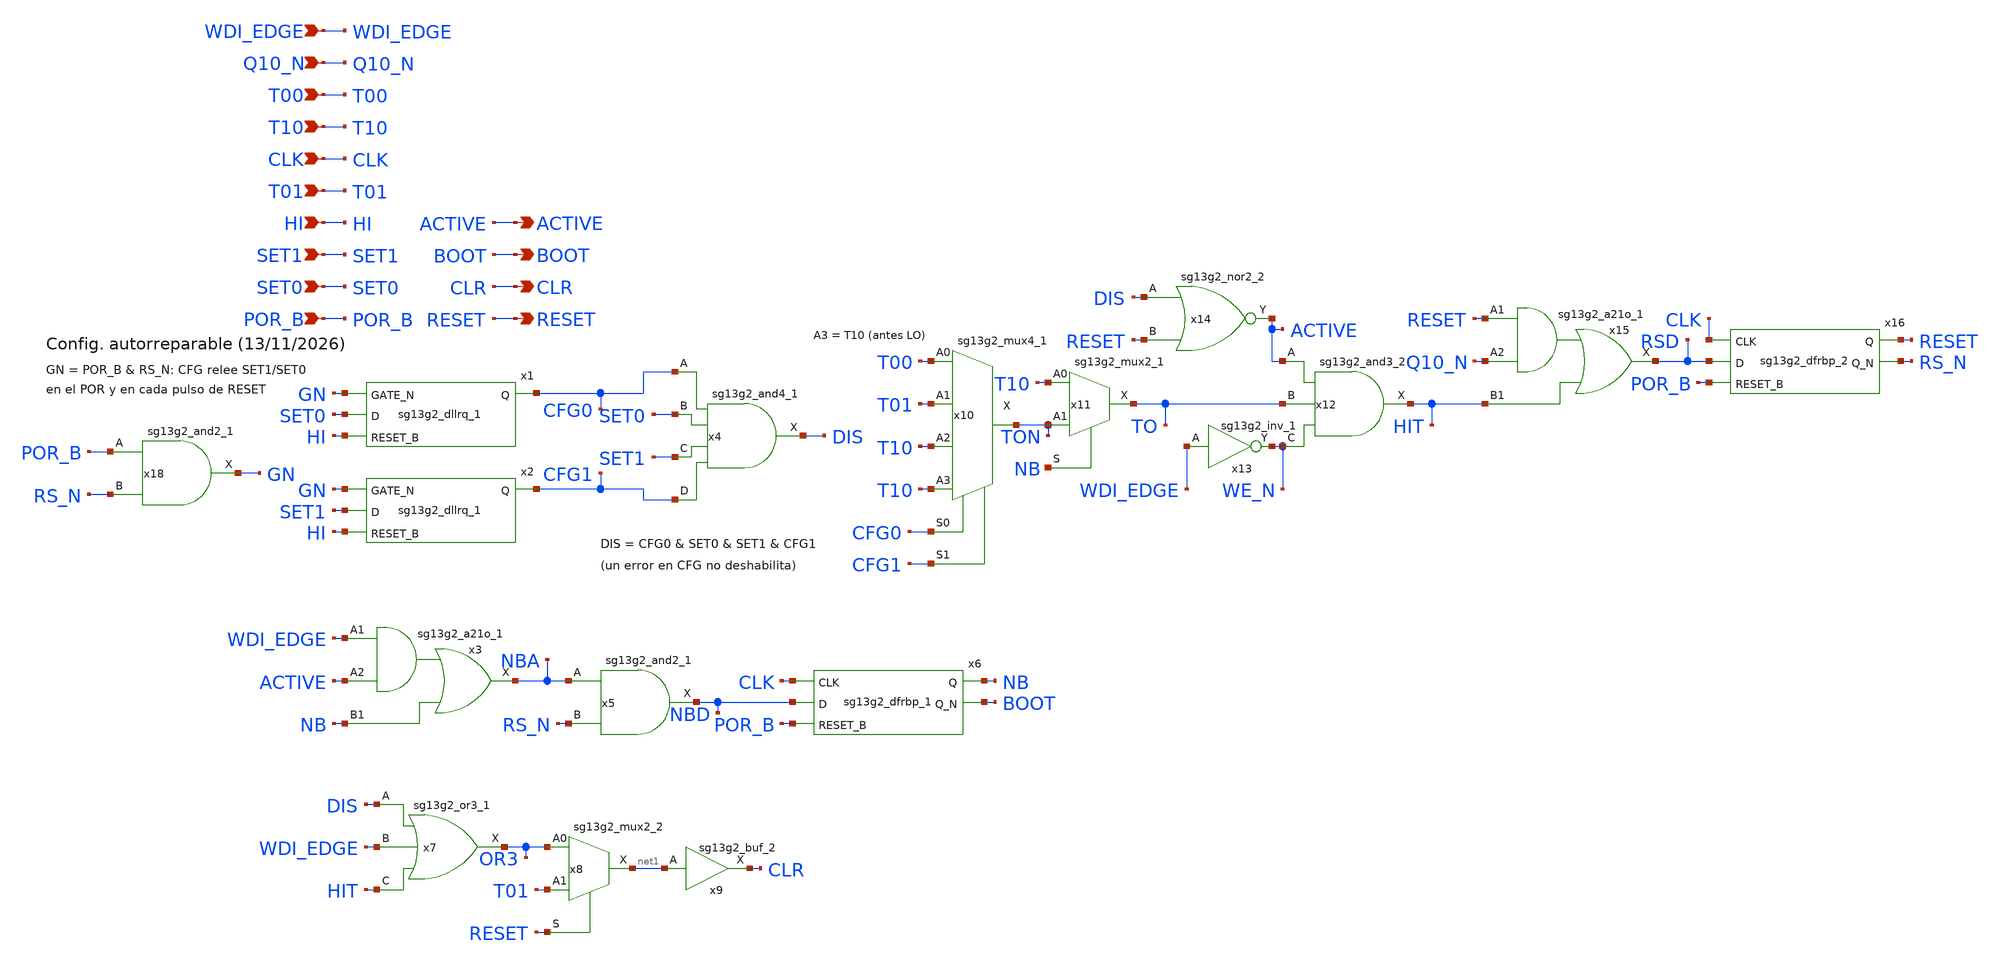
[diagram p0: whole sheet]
** sch_path: design/blocks/digital/schematic/wd_control.sch
* IHP-GmbH/IHP-Open-PDK/ihp-sg13g2/libs.tech/xschem/sg13g2_stdcells/sg13g2_a21o_1.sch:
* Copyright 2023 IHP PDK Authors
* Licensed under the Apache License, Version 2.0 (the "License");
**.subckt wd_control POR_B SET0 CLR RESET SET1 HI T01 ACTIVE BOOT CLK T10 T00 Q10_N WDI_EDGE
*.ipin POR_B
*.ipin SET0
*.opin CLR
*.opin RESET
*.ipin SET1
*.ipin HI
*.ipin T01
*.opin ACTIVE
*.opin BOOT
*.ipin CLK
*.ipin T10
*.ipin T00
*.ipin Q10_N
*.ipin WDI_EDGE
x1 SET0 HI VGND VNB VPB VPWR CFG0 sg13g2_dllrq_1
x2 SET1 HI VGND VNB VPB VPWR CFG1 sg13g2_dllrq_1
x3 NBA WDI_EDGE ACTIVE NB VDD VSS sg13g2_a21o_1
x5 NBD NBA RS_N VDD VSS sg13g2_and2_1
x6 NB BOOT CLK NBD POR_B VDD VSS sg13g2_dfrbp_1
x7 OR3 DIS WDI_EDGE HIT VDD VSS sg13g2_or3_1
x8 net1 OR3 T01 RESET VDD VSS sg13g2_mux2_2
x9 CLR net1 VDD VSS sg13g2_buf_2
x10 TON T00 T01 T10 T10 CFG0 CFG1 VDD VSS sg13g2_mux4_1
x11 TO T10 TON NB VDD VSS sg13g2_mux2_1
x12 HIT ACTIVE TO WE_N VDD VSS sg13g2_and3_2
x13 WE_N WDI_EDGE VDD VSS sg13g2_inv_1
x14 ACTIVE DIS RESET VDD VSS sg13g2_nor2_2
x15 RSD RESET Q10_N HIT VDD VSS sg13g2_a21o_1
x16 RESET RS_N CLK RSD POR_B VDD VSS sg13g2_dfrbp_2
x4 DIS CFG0 SET0 SET1 CFG1 VDD VSS sg13g2_and4_1
x18 GN POR_B RS_N VDD VSS sg13g2_and2_1
**.ends

* expanding   symbol:  sg13g2_a21o_1.sym # of pins=4
** sym_path: sg13g2_a21o_1.sym
** sch_path: sg13g2_a21o_1.sch
.subckt sg13g2_a21o_1 X A1 A2 B1 VDD VSS
*.opin X
*.ipin A1
*.ipin A2
*.ipin B1
*.iopin VDD
*.iopin VSS
XM1 net1 A1 net3 VSS sg13_lv_nmos w=640.00n l=130.00n ng=1 m=1 mm_ok=1
XM2 net3 A2 VSS VSS sg13_lv_nmos w=640.00n l=130.00n ng=1 m=1 mm_ok=1
XM3 net1 B1 VSS VSS sg13_lv_nmos w=640.00n l=130.00n ng=1 m=1 mm_ok=1
XM4 X net1 VSS VSS sg13_lv_nmos w=740.00n l=130.00n ng=1 m=1 mm_ok=1
XM5 net2 A1 VDD VDD sg13_lv_pmos w=1.000u l=130.00n ng=1 m=1 mm_ok=1
XM6 net2 A2 VDD VDD sg13_lv_pmos w=1.000u l=130.00n ng=1 m=1 mm_ok=1
XM7 net1 B1 net2 VDD sg13_lv_pmos w=1.000u l=130.00n ng=1 m=1 mm_ok=1
XM8 X net1 VDD VDD sg13_lv_pmos w=1.12u l=130.00n ng=1 m=1 mm_ok=1
.ends


* expanding   symbol:  sg13g2_and2_1.sym # of pins=3
** sym_path: sg13g2_and2_1.sym
** sch_path: sg13g2_and2_1.sch
.subckt sg13g2_and2_1 X A B VDD VSS
*.ipin A
*.ipin B
*.opin X
*.iopin VDD
*.iopin VSS
XM1 net1 A net2 VSS sg13_lv_nmos w=640.00n l=130.00n ng=1 m=1 mm_ok=1
XM2 net2 B VSS VSS sg13_lv_nmos w=640.00n l=130.00n ng=1 m=1 mm_ok=1
XM3 X net1 VSS VSS sg13_lv_nmos w=740.00n l=130.00n ng=1 m=1 mm_ok=1
XM4 net1 B VDD VDD sg13_lv_pmos w=840.00n l=130.00n ng=1 m=1 mm_ok=1
XM5 net1 A VDD VDD sg13_lv_pmos w=840.00n l=130.00n ng=1 m=1 mm_ok=1
XM6 X net1 VDD VDD sg13_lv_pmos w=1.12u l=130.00n ng=1 m=1 mm_ok=1
.ends


* expanding   symbol:  sg13g2_dfrbp_1.sym # of pins=5
** sym_path: sg13g2_dfrbp_1.sym
** sch_path: sg13g2_dfrbp_1.sch
.subckt sg13g2_dfrbp_1 Q Q_N CLK D RESET_B VDD VSS
*.ipin D
*.ipin RESET_B
*.ipin CLK
*.opin Q
*.opin Q_N
*.iopin VDD
*.iopin VSS
XM1 Db D net10 VSS sg13_lv_nmos w=420.00n l=130.00n ng=1 m=1 mm_ok=1
XM2 net10 RESET_B VSS VSS sg13_lv_nmos w=420.00n l=130.00n ng=1 m=1 mm_ok=1
XM3 net1 clkneg net9 VSS sg13_lv_nmos w=420.00n l=130.00n ng=1 m=1 mm_ok=1
XM4 net9 net1 VSS VSS sg13_lv_nmos w=420.00n l=130.00n ng=1 m=1 mm_ok=1
XM5 net1 net1 net5 VSS sg13_lv_nmos w=420.00n l=130.00n ng=1 m=1 mm_ok=1
XM6 net5 RESET_B VSS VSS sg13_lv_nmos w=420.00n l=130.00n ng=1 m=1 mm_ok=1
XM7 Q_N net1 VSS VSS sg13_lv_nmos w=740.00n l=130.00n ng=1 m=1 mm_ok=1
XM8 net2 net1 VSS VSS sg13_lv_nmos w=740.00n l=130.00n ng=1 m=1 mm_ok=1
XM9 Q net2 VSS VSS sg13_lv_nmos w=740.00n l=130.00n ng=1 m=1 mm_ok=1
XM10 clkneg CLK VSS VSS sg13_lv_nmos w=740.00n l=130.00n ng=1 m=1 mm_ok=1
XM11 clkpos clkneg VSS VSS sg13_lv_nmos w=740.00n l=130.00n ng=1 m=1 mm_ok=1
XM12 Db clkneg net3 VSS sg13_lv_nmos w=420.00n l=130.00n ng=1 m=1 mm_ok=1
XM13 net3 clkpos net8 VSS sg13_lv_nmos w=420.00n l=130.00n ng=1 m=1 mm_ok=1
XM14 net8 net3 net4 VSS sg13_lv_nmos w=420.00n l=130.00n ng=1 m=1 mm_ok=1
XM15 net4 RESET_B VSS VSS sg13_lv_nmos w=420.00n l=130.00n ng=1 m=1 mm_ok=1
XM16 net3 net3 VSS VSS sg13_lv_nmos w=740.00n l=130.00n ng=1 m=1 mm_ok=1
XM17 net3 clkpos net1 VSS sg13_lv_nmos w=740.00n l=130.00n ng=1 m=1 mm_ok=1
XM18 Db RESET_B VDD VDD sg13_lv_pmos w=420.00n l=130.00n ng=1 m=1 mm_ok=1
XM19 Db D VDD VDD sg13_lv_pmos w=420.00n l=130.00n ng=1 m=1 mm_ok=1
XM20 net7 net1 VDD VDD sg13_lv_pmos w=420.00n l=130.00n ng=1 m=1 mm_ok=1
XM21 net1 clkpos net7 VDD sg13_lv_pmos w=420.00n l=130.00n ng=1 m=1 mm_ok=1
XM22 net1 net1 VDD VDD sg13_lv_pmos w=420.00n l=130.00n ng=1 m=1 mm_ok=1
XM23 net1 RESET_B VDD VDD sg13_lv_pmos w=420.00n l=130.00n ng=1 m=1 mm_ok=1
XM24 Q_N net1 VDD VDD sg13_lv_pmos w=1.12u l=130.00n ng=1 m=1 mm_ok=1
XM25 net2 net1 VDD VDD sg13_lv_pmos w=1.12u l=130.00n ng=1 m=1 mm_ok=1
XM26 Q net2 VDD VDD sg13_lv_pmos w=1.12u l=130.00n ng=1 m=1 mm_ok=1
XM27 clkneg CLK VDD VDD sg13_lv_pmos w=1.12u l=130.00n ng=1 m=1 mm_ok=1
XM28 clkpos clkneg VDD VDD sg13_lv_pmos w=1.12u l=130.00n ng=1 m=1 mm_ok=1
XM29 Db clkpos net3 VDD sg13_lv_pmos w=420.00n l=130.00n ng=1 m=1 mm_ok=1
XM30 net6 net3 VDD VDD sg13_lv_pmos w=420.00n l=130.00n ng=1 m=1 mm_ok=1
XM31 net3 clkneg net6 VDD sg13_lv_pmos w=420.00n l=130.00n ng=1 m=1 mm_ok=1
XM32 net3 RESET_B VDD VDD sg13_lv_pmos w=420.00n l=130.00n ng=1 m=1 mm_ok=1
XM33 net3 net3 VDD VDD sg13_lv_pmos w=1.000u l=130.00n ng=1 m=1 mm_ok=1
XM34 net3 clkneg net1 VDD sg13_lv_pmos w=1.000u l=130.00n ng=1 m=1 mm_ok=1
.ends


* expanding   symbol:  sg13g2_or3_1.sym # of pins=4
** sym_path: sg13g2_or3_1.sym
** sch_path: sg13g2_or3_1.sch
.subckt sg13g2_or3_1 X A B C VDD VSS
*.opin X
*.ipin C
*.ipin B
*.ipin A
*.iopin VDD
*.iopin VSS
XM1 net2 A VSS VSS sg13_lv_nmos w=550.00n l=130.00n ng=1 m=1 mm_ok=1
XM2 net2 B VSS VSS sg13_lv_nmos w=550.00n l=130.00n ng=1 m=1 mm_ok=1
XM3 net2 C VSS VSS sg13_lv_nmos w=550.00n l=130.00n ng=1 m=1 mm_ok=1
XM4 X net2 VSS VSS sg13_lv_nmos w=740.00n l=130.00n ng=1 m=1 mm_ok=1
XM5 net1 A VDD VDD sg13_lv_pmos w=1.000u l=130.00n ng=1 m=1 mm_ok=1
XM6 net3 B net1 VDD sg13_lv_pmos w=1.000u l=130.00n ng=1 m=1 mm_ok=1
XM7 net2 C net3 VDD sg13_lv_pmos w=1.000u l=130.00n ng=1 m=1 mm_ok=1
XM8 X net2 VDD VDD sg13_lv_pmos w=1.12u l=130.00n ng=1 m=1 mm_ok=1
.ends


* expanding   symbol:  sg13g2_mux2_2.sym # of pins=4
** sym_path: sg13g2_mux2_2.sym
** sch_path: sg13g2_mux2_2.sch
.subckt sg13g2_mux2_2 X A0 A1 S VDD VSS
*.ipin S
*.ipin A0
*.ipin A1
*.opin X
*.iopin VDD
*.iopin VSS
XM1 Sb S VSS VSS sg13_lv_nmos w=550.00n l=130.00n ng=1 m=1 mm_ok=1
XM2 net1 A0 net5 VSS sg13_lv_nmos w=740.00n l=130.00n ng=1 m=1 mm_ok=1
XM3 net5 Sb VSS VSS sg13_lv_nmos w=740.00n l=130.00n ng=1 m=1 mm_ok=1
XM4 net1 A1 net4 VSS sg13_lv_nmos w=740.00n l=130.00n ng=1 m=1 mm_ok=1
XM5 net4 S VSS VSS sg13_lv_nmos w=740.00n l=130.00n ng=1 m=1 mm_ok=1
XM6 X net1 VSS VSS sg13_lv_nmos w=1.48u l=130.00n ng=2 m=1 mm_ok=1
XM7 Sb S VDD VDD sg13_lv_pmos w=840.00n l=130.00n ng=1 m=1 mm_ok=1
XM8 net2 S VDD VDD sg13_lv_pmos w=1.000u l=130.00n ng=1 m=1 mm_ok=1
XM9 net1 A0 net2 VDD sg13_lv_pmos w=1.000u l=130.00n ng=1 m=1 mm_ok=1
XM10 net3 Sb VDD VDD sg13_lv_pmos w=1.000u l=130.00n ng=1 m=1 mm_ok=1
XM11 net1 A1 net3 VDD sg13_lv_pmos w=1.000u l=130.00n ng=1 m=1 mm_ok=1
XM12 X net1 VDD VDD sg13_lv_pmos w=2.24u l=130.00n ng=2 m=1 mm_ok=1
.ends


* expanding   symbol:  sg13g2_buf_2.sym # of pins=2
** sym_path: sg13g2_buf_2.sym
** sch_path: sg13g2_buf_2.sch
.subckt sg13g2_buf_2 X A VDD VSS
*.ipin A
*.opin X
*.iopin VDD
*.iopin VSS
XM1 net1 A VSS VSS sg13_lv_nmos w=640.00n l=130.00n ng=1 m=1 mm_ok=1
XM2 X net1 VSS VSS sg13_lv_nmos w=1.48u l=130.00n ng=2 m=1 mm_ok=1
XM3 net1 A VDD VDD sg13_lv_pmos w=1.000u l=130.00n ng=1 m=1 mm_ok=1
XM4 X net1 VDD VDD sg13_lv_pmos w=2.24u l=130.00n ng=2 m=1 mm_ok=1
.ends


* expanding   symbol:  sg13g2_mux4_1.sym # of pins=7
** sym_path: sg13g2_mux4_1.sym
** sch_path: sg13g2_mux4_1.sch
.subckt sg13g2_mux4_1 X A0 A1 A2 A3 S0 S1 VDD VSS
*.ipin S0
*.ipin S1
*.iopin VSS
*.ipin A0
*.ipin A1
*.ipin A2
*.ipin A3
*.opin X
*.iopin VDD
XM1 S0b S0 VSS VSS sg13_lv_nmos w=640.00n l=130.00n ng=1 m=1 mm_ok=1
XM2 S1b S1 VSS VSS sg13_lv_nmos w=640.00n l=130.00n ng=1 m=1 mm_ok=1
XM3 net4 A3 VSS VSS sg13_lv_nmos w=640.00n l=130.00n ng=1 m=1 mm_ok=1
XM4 high S1 Xb VSS sg13_lv_nmos w=640.00n l=130.00n ng=1 m=1 mm_ok=1
XM5 X Xb VSS VSS sg13_lv_nmos w=740.00n l=130.00n ng=1 m=1 mm_ok=1
XM6 low S0b net7 VSS sg13_lv_nmos w=640.00n l=130.00n ng=1 m=1 mm_ok=1
XM7 net7 A0 VSS VSS sg13_lv_nmos w=640.00n l=130.00n ng=1 m=1 mm_ok=1
XM8 low S0 net2 VSS sg13_lv_nmos w=640.00n l=130.00n ng=1 m=1 mm_ok=1
XM9 net2 A1 VSS VSS sg13_lv_nmos w=640.00n l=130.00n ng=1 m=1 mm_ok=1
XM10 low S1b Xb VSS sg13_lv_nmos w=640.00n l=130.00n ng=1 m=1 mm_ok=1
XM11 high S0b net6 VSS sg13_lv_nmos w=640.00n l=130.00n ng=1 m=1 mm_ok=1
XM12 net6 A2 VSS VSS sg13_lv_nmos w=640.00n l=130.00n ng=1 m=1 mm_ok=1
XM13 high S0 net4 VSS sg13_lv_nmos w=640.00n l=130.00n ng=1 m=1 mm_ok=1
XM14 S0b S0 VDD VDD sg13_lv_pmos w=1.000u l=130.00n ng=1 m=1 mm_ok=1
XM15 S1b S1 VDD VDD sg13_lv_pmos w=1.000u l=130.00n ng=1 m=1 mm_ok=1
XM16 high S0b net3 VDD sg13_lv_pmos w=1.000u l=130.00n ng=1 m=1 mm_ok=1
XM17 high S1b Xb VDD sg13_lv_pmos w=1.000u l=130.00n ng=1 m=1 mm_ok=1
XM18 X Xb VDD VDD sg13_lv_pmos w=1.12u l=130.00n ng=1 m=1 mm_ok=1
XM19 net8 A0 VDD VDD sg13_lv_pmos w=1.000u l=130.00n ng=1 m=1 mm_ok=1
XM20 low S0 net8 VDD sg13_lv_pmos w=1.000u l=130.00n ng=1 m=1 mm_ok=1
XM21 net1 A1 VDD VDD sg13_lv_pmos w=1.000u l=130.00n ng=1 m=1 mm_ok=1
XM22 low S0b net1 VDD sg13_lv_pmos w=1.000u l=130.00n ng=1 m=1 mm_ok=1
XM23 low S1 Xb VDD sg13_lv_pmos w=1.000u l=130.00n ng=1 m=1 mm_ok=1
XM24 net5 A2 VDD VDD sg13_lv_pmos w=1.000u l=130.00n ng=1 m=1 mm_ok=1
XM25 high S0 net5 VDD sg13_lv_pmos w=1.000u l=130.00n ng=1 m=1 mm_ok=1
XM26 net3 A3 VDD VDD sg13_lv_pmos w=1.000u l=130.00n ng=1 m=1 mm_ok=1
.ends


* expanding   symbol:  sg13g2_mux2_1.sym # of pins=4
** sym_path: sg13g2_mux2_1.sym
** sch_path: sg13g2_mux2_1.sch
.subckt sg13g2_mux2_1 X A0 A1 S VDD VSS
*.ipin S
*.ipin A0
*.ipin A1
*.opin X
*.iopin VDD
*.iopin VSS
XM1 Sb S VSS VSS sg13_lv_nmos w=550.00n l=130.00n ng=1 m=1 mm_ok=1
XM2 net1 A0 net5 VSS sg13_lv_nmos w=740.00n l=130.00n ng=1 m=1 mm_ok=1
XM3 net5 Sb VSS VSS sg13_lv_nmos w=740.00n l=130.00n ng=1 m=1 mm_ok=1
XM4 net1 A1 net4 VSS sg13_lv_nmos w=740.00n l=130.00n ng=1 m=1 mm_ok=1
XM5 net4 S VSS VSS sg13_lv_nmos w=740.00n l=130.00n ng=1 m=1 mm_ok=1
XM6 X net1 VSS VSS sg13_lv_nmos w=740.00n l=130.00n ng=1 m=1 mm_ok=1
XM7 Sb S VDD VDD sg13_lv_pmos w=840.00n l=130.00n ng=1 m=1 mm_ok=1
XM8 net2 S VDD VDD sg13_lv_pmos w=1.000u l=130.00n ng=1 m=1 mm_ok=1
XM9 net1 A0 net2 VDD sg13_lv_pmos w=1.000u l=130.00n ng=1 m=1 mm_ok=1
XM10 net3 Sb VDD VDD sg13_lv_pmos w=1.000u l=130.00n ng=1 m=1 mm_ok=1
XM11 net1 A1 net3 VDD sg13_lv_pmos w=1.000u l=130.00n ng=1 m=1 mm_ok=1
XM12 X net1 VDD VDD sg13_lv_pmos w=1.12u l=130.00n ng=1 m=1 mm_ok=1
.ends


* expanding   symbol:  sg13g2_and3_2.sym # of pins=4
** sym_path: sg13g2_and3_2.sym
** sch_path: sg13g2_and3_2.sch
.subckt sg13g2_and3_2 X A B C VDD VSS
*.opin X
*.ipin C
*.ipin B
*.ipin A
*.iopin VDD
*.iopin VSS
XM1 net1 A net3 VSS sg13_lv_nmos w=640.00n l=130.00n ng=1 m=1 mm_ok=1
XM2 net3 B net2 VSS sg13_lv_nmos w=640.00n l=130.00n ng=1 m=1 mm_ok=1
XM3 net2 C VSS VSS sg13_lv_nmos w=640.00n l=130.00n ng=1 m=1 mm_ok=1
XM4 X net1 VSS VSS sg13_lv_nmos w=1.48u l=130.00n ng=2 m=1 mm_ok=1
XM5 net1 C VDD VDD sg13_lv_pmos w=840.00n l=130.00n ng=1 m=1 mm_ok=1
XM6 net1 B VDD VDD sg13_lv_pmos w=840.00n l=130.00n ng=1 m=1 mm_ok=1
XM7 net1 A VDD VDD sg13_lv_pmos w=840.00n l=130.00n ng=1 m=1 mm_ok=1
XM8 X net1 VDD VDD sg13_lv_pmos w=2.24u l=130.00n ng=2 m=1 mm_ok=1
.ends


* expanding   symbol:  sg13g2_inv_1.sym # of pins=2
** sym_path: sg13g2_inv_1.sym
** sch_path: sg13g2_inv_1.sch
.subckt sg13g2_inv_1 Y A VDD VSS
*.opin Y
*.ipin A
*.iopin VDD
*.iopin VSS
XM1 Y A VSS VSS sg13_lv_nmos w=740.00n l=130.00n ng=1 m=1 mm_ok=1
XM2 Y A VDD VDD sg13_lv_pmos w=1.12u l=130.00n ng=1 m=1 mm_ok=1
.ends


* expanding   symbol:  sg13g2_nor2_2.sym # of pins=3
** sym_path: sg13g2_nor2_2.sym
** sch_path: sg13g2_nor2_2.sch
.subckt sg13g2_nor2_2 Y A B VDD VSS
*.opin Y
*.ipin B
*.ipin A
*.iopin VDD
*.iopin VSS
XM1 Y A VSS VSS sg13_lv_nmos w=1.48u l=130.00n ng=2 m=1 mm_ok=1
XM2 Y B VSS VSS sg13_lv_nmos w=1.48u l=130.00n ng=2 m=1 mm_ok=1
XM3 net1 A VDD VDD sg13_lv_pmos w=2.24u l=130.00n ng=2 m=1 mm_ok=1
XM4 Y B net1 VDD sg13_lv_pmos w=2.24u l=130.00n ng=2 m=1 mm_ok=1
.ends


* expanding   symbol:  sg13g2_dfrbp_2.sym # of pins=5
** sym_path: sg13g2_dfrbp_2.sym
** sch_path: sg13g2_dfrbp_2.sch
.subckt sg13g2_dfrbp_2 Q Q_N CLK D RESET_B VDD VSS
*.ipin D
*.ipin RESET_B
*.ipin CLK
*.opin Q
*.opin Q_N
*.iopin VDD
*.iopin VSS
XM1 Db D net12 VSS sg13_lv_nmos w=420.00n l=130.00n ng=1 m=1 mm_ok=1
XM2 net12 RESET_B VSS VSS sg13_lv_nmos w=420.00n l=130.00n ng=1 m=1 mm_ok=1
XM3 net2 clkneg net11 VSS sg13_lv_nmos w=420.00n l=130.00n ng=1 m=1 mm_ok=1
XM4 net11 net3 VSS VSS sg13_lv_nmos w=420.00n l=130.00n ng=1 m=1 mm_ok=1
XM5 net3 net2 net7 VSS sg13_lv_nmos w=420.00n l=130.00n ng=1 m=1 mm_ok=1
XM6 net7 RESET_B VSS VSS sg13_lv_nmos w=420.00n l=130.00n ng=1 m=1 mm_ok=1
XM7 Q_N net2 VSS VSS sg13_lv_nmos w=1.48u l=130.00n ng=2 m=1 mm_ok=1
XM8 net1 net2 VSS VSS sg13_lv_nmos w=640.00n l=130.00n ng=1 m=1 mm_ok=1
XM9 Q net1 VSS VSS sg13_lv_nmos w=1.48u l=130.00n ng=2 m=1 mm_ok=1
XM10 clkneg CLK VSS VSS sg13_lv_nmos w=740.00n l=130.00n ng=1 m=1 mm_ok=1
XM11 clkpos clkneg VSS VSS sg13_lv_nmos w=740.00n l=130.00n ng=1 m=1 mm_ok=1
XM12 Db clkneg net4 VSS sg13_lv_nmos w=420.00n l=130.00n ng=1 m=1 mm_ok=1
XM13 net4 clkpos net10 VSS sg13_lv_nmos w=420.00n l=130.00n ng=1 m=1 mm_ok=1
XM14 net10 net5 net6 VSS sg13_lv_nmos w=420.00n l=130.00n ng=1 m=1 mm_ok=1
XM15 net6 RESET_B VSS VSS sg13_lv_nmos w=420.00n l=130.00n ng=1 m=1 mm_ok=1
XM16 net5 net4 VSS VSS sg13_lv_nmos w=740.00n l=130.00n ng=1 m=1 mm_ok=1
XM17 net5 clkpos net2 VSS sg13_lv_nmos w=740.00n l=130.00n ng=1 m=1 mm_ok=1
XM18 Db RESET_B VDD VDD sg13_lv_pmos w=420.00n l=130.00n ng=1 m=1 mm_ok=1
XM19 Db D VDD VDD sg13_lv_pmos w=420.00n l=130.00n ng=1 m=1 mm_ok=1
XM20 net9 net3 VDD VDD sg13_lv_pmos w=420.00n l=130.00n ng=1 m=1 mm_ok=1
XM21 net2 clkpos net9 VDD sg13_lv_pmos w=420.00n l=130.00n ng=1 m=1 mm_ok=1
XM22 net3 net2 VDD VDD sg13_lv_pmos w=420.00n l=130.00n ng=1 m=1 mm_ok=1
XM23 net3 RESET_B VDD VDD sg13_lv_pmos w=420.00n l=130.00n ng=1 m=1 mm_ok=1
XM24 Q_N net2 VDD VDD sg13_lv_pmos w=2.24u l=130.00n ng=2 m=1 mm_ok=1
XM25 net1 net2 VDD VDD sg13_lv_pmos w=1.000u l=130.00n ng=1 m=1 mm_ok=1
XM26 Q net1 VDD VDD sg13_lv_pmos w=2.24u l=130.00n ng=2 m=1 mm_ok=1
XM27 clkneg CLK VDD VDD sg13_lv_pmos w=1.12u l=130.00n ng=1 m=1 mm_ok=1
XM28 clkpos clkneg VDD VDD sg13_lv_pmos w=1.12u l=130.00n ng=1 m=1 mm_ok=1
XM29 Db clkpos net4 VDD sg13_lv_pmos w=420.00n l=130.00n ng=1 m=1 mm_ok=1
XM30 net8 net5 VDD VDD sg13_lv_pmos w=420.00n l=130.00n ng=1 m=1 mm_ok=1
XM31 net4 clkneg net8 VDD sg13_lv_pmos w=420.00n l=130.00n ng=1 m=1 mm_ok=1
XM32 net4 RESET_B VDD VDD sg13_lv_pmos w=420.00n l=130.00n ng=1 m=1 mm_ok=1
XM33 net5 net4 VDD VDD sg13_lv_pmos w=1.000u l=130.00n ng=1 m=1 mm_ok=1
XM34 net5 clkneg net2 VDD sg13_lv_pmos w=1.000u l=130.00n ng=1 m=1 mm_ok=1
.ends


* expanding   symbol:  sg13g2_and4_1.sym # of pins=5
** sym_path: sg13g2_and4_1.sym
** sch_path: sg13g2_and4_1.sch
.subckt sg13g2_and4_1 X A B C D VDD VSS
*.ipin A
*.ipin B
*.ipin C
*.ipin D
*.opin X
*.iopin VDD
*.iopin VSS
XM1 net1 A net3 VSS sg13_lv_nmos w=640.00n l=130.00n ng=1 m=1 mm_ok=1
XM2 net3 B net2 VSS sg13_lv_nmos w=640.00n l=130.00n ng=1 m=1 mm_ok=1
XM3 net2 C net4 VSS sg13_lv_nmos w=640.00n l=130.00n ng=1 m=1 mm_ok=1
XM4 net4 D VSS VSS sg13_lv_nmos w=640.00n l=130.00n ng=1 m=1 mm_ok=1
XM5 X net1 VSS VSS sg13_lv_nmos w=740.00n l=130.00n ng=1 m=1 mm_ok=1
XM6 net1 D VDD VDD sg13_lv_pmos w=840.00n l=130.00n ng=1 m=1 mm_ok=1
XM7 net1 C VDD VDD sg13_lv_pmos w=840.00n l=130.00n ng=1 m=1 mm_ok=1
XM8 net1 B VDD VDD sg13_lv_pmos w=840.00n l=130.00n ng=1 m=1 mm_ok=1
XM9 net1 A VDD VDD sg13_lv_pmos w=840.00n l=130.00n ng=1 m=1 mm_ok=1
XM10 X net1 VDD VDD sg13_lv_pmos w=1.12u l=130.00n ng=1 m=1 mm_ok=1
.ends

.end
